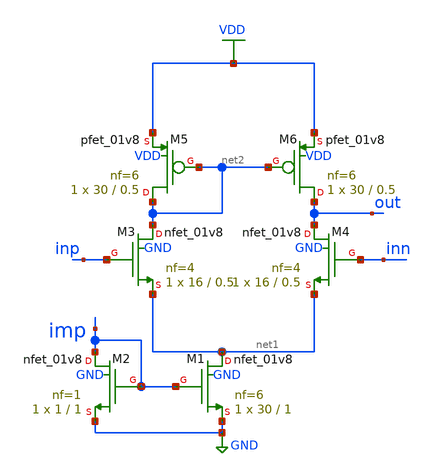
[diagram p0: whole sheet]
** sch_path: netlists/ota.sch
**.subckt ota
XM1 net1 imp GND GND sky130_fd_pr__nfet_01v8 L=1 W=30 nf=6 ad='int((nf+1)/2) * W/nf * 0.29' as='int((nf+2)/2) * W/nf * 0.29'
+ pd='2*int((nf+1)/2) * (W/nf + 0.29)' ps='2*int((nf+2)/2) * (W/nf + 0.29)' nrd='0.29 / W' nrs='0.29 / W'
+ sa=0 sb=0 sd=0 mult=1 m=1
XM2 imp imp GND GND sky130_fd_pr__nfet_01v8 L=1 W=1 nf=1 ad='int((nf+1)/2) * W/nf * 0.29' as='int((nf+2)/2) * W/nf * 0.29'
+ pd='2*int((nf+1)/2) * (W/nf + 0.29)' ps='2*int((nf+2)/2) * (W/nf + 0.29)' nrd='0.29 / W' nrs='0.29 / W'
+ sa=0 sb=0 sd=0 mult=1 m=1
XM3 net2 inp net1 GND sky130_fd_pr__nfet_01v8 L=0.5 W=16 nf=4 ad='int((nf+1)/2) * W/nf * 0.29' as='int((nf+2)/2) * W/nf * 0.29'
+ pd='2*int((nf+1)/2) * (W/nf + 0.29)' ps='2*int((nf+2)/2) * (W/nf + 0.29)' nrd='0.29 / W' nrs='0.29 / W'
+ sa=0 sb=0 sd=0 mult=1 m=1
XM4 out inn net1 GND sky130_fd_pr__nfet_01v8 L=0.5 W=16 nf=4 ad='int((nf+1)/2) * W/nf * 0.29' as='int((nf+2)/2) * W/nf * 0.29'
+ pd='2*int((nf+1)/2) * (W/nf + 0.29)' ps='2*int((nf+2)/2) * (W/nf + 0.29)' nrd='0.29 / W' nrs='0.29 / W'
+ sa=0 sb=0 sd=0 mult=1 m=1
XM5 net2 net2 VDD VDD sky130_fd_pr__pfet_01v8 L=0.5 W=30 nf=6 ad='int((nf+1)/2) * W/nf * 0.29' as='int((nf+2)/2) * W/nf * 0.29'
+ pd='2*int((nf+1)/2) * (W/nf + 0.29)' ps='2*int((nf+2)/2) * (W/nf + 0.29)' nrd='0.29 / W' nrs='0.29 / W'
+ sa=0 sb=0 sd=0 mult=1 m=1
XM6 out net2 VDD VDD sky130_fd_pr__pfet_01v8 L=0.5 W=30 nf=6 ad='int((nf+1)/2) * W/nf * 0.29' as='int((nf+2)/2) * W/nf * 0.29'
+ pd='2*int((nf+1)/2) * (W/nf + 0.29)' ps='2*int((nf+2)/2) * (W/nf + 0.29)' nrd='0.29 / W' nrs='0.29 / W'
+ sa=0 sb=0 sd=0 mult=1 m=1
**.ends
.GLOBAL VDD
.GLOBAL GND
.end
